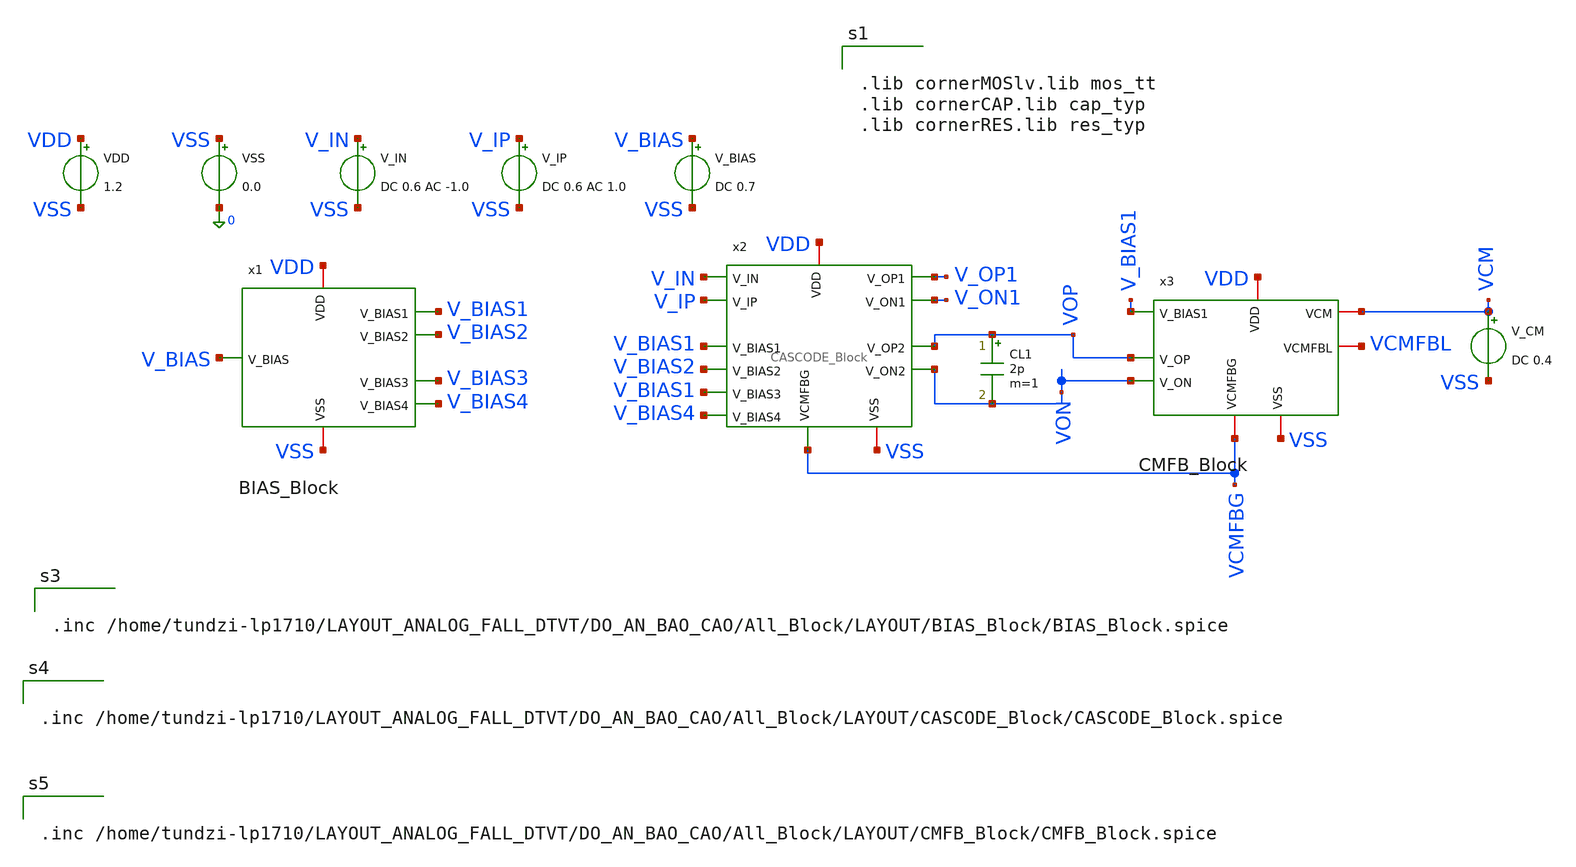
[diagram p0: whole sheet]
** sch_path: two-stage-ota-with-cmfb/Layout_PEX_PostSimulation/LAYOUT/SCHEMATIC_FOR_LAYOUT/All_Block_LAYOUT.sch
**.subckt All_Block_LAYOUT
VDD VDD VSS 1.2
VSS VSS 0 0.0
V_IN V_IN VSS DC 0.6 AC -1.0
V_IP V_IP VSS DC 0.6 AC 1.0
V_BIAS V_BIAS VSS DC 0.7
V_CM VCM VSS DC 0.4
CL1 VOP VON 2p m=1
x1 VDD VSS V_BIAS4 V_BIAS2 V_BIAS3 V_BIAS1 V_BIAS BIAS_Block
x2 VON VOP V_ON1 V_OP1 V_IN V_IP V_BIAS1 VSS V_BIAS4 V_BIAS1 VCMFBG VDD V_BIAS2 CASCODE_Block
x3 VDD V_BIAS1 VOP VON VCM VCMFBG VCMFBL VSS CMFB_Block
**** begin user architecture code


.lib cornerMOSlv.lib mos_tt
.lib cornerCAP.lib cap_typ
.lib cornerRES.lib res_typ




.control
unset echo
set color0=white
set color1=black

* ============================================================
* 1. DC, CONG SUAT & OUTPUT COMMON-MODE
* ============================================================
op
let p_total = -v(VDD)*i(vdd)
let vocm = 0.5 * (v(vop) + v(von))
set r_vocm = $&vocm
set r_ptotal = $&p_total

* ============================================================
* 2. AC VI SAI: GAIN, GBW, PHASE MARGIN
* ============================================================
alter @v_ip[acmag] = 0.5
alter @v_in[acmag] = -0.5
alter @vdd[acmag] = 0

ac dec 50 1 10G
let vod = v(vop) - v(von)
let vid = v(v_ip) - v(v_in)
let gain_db = db(vod/vid)
let phase_deg = 180/PI * cph(vod/vid)

meas ac adm_dc find gain_db at=1
meas ac GBW when gain_db=0
meas ac Phase_at_GBW find phase_deg at=GBW
let Phase_Margin = 180 + Phase_at_GBW

set r_gain = $&adm_dc
set r_gbw_mhz = $&GBW
set r_pm = $&Phase_Margin

* ============================================================
* 3. NOISE NGO VAO TAI 1 MHz (DA SUA TRIET DE LOI SCALAR)
* ============================================================
noise v(vop,von) v_ip dec 10 1Meg 1Meg
let noise_val = noise1.inoise_spectrum
set r_noise = $&noise_val

* ============================================================
* 4. CMRR TAI DC
* ============================================================
alter @v_ip[acmag] = 1.0
alter @v_in[acmag] = 1.0
alter @vdd[acmag] = 0

ac dec 20 1 10Meg
let vocm_ac = 0.5 * (v(vop) + v(von))
let vicm_ac = v(v_ip)
let acm_db = db(vocm_ac / vicm_ac)
let cmrr_val = $r_gain - acm_db[0]
set r_cmrr = $&cmrr_val

* ============================================================
* 5. PSRR TAI DC
* ============================================================
alter @v_ip[acmag] = 0
alter @v_in[acmag] = 0
alter @vdd[acmag] = 1.0

ac dec 20 1 10Meg
let vod_psrr = v(vop) - v(von)
let asupply_db = db(vod_psrr)
let psrr_val = $r_gain - asupply_db[0]
set r_psrr = $&psrr_val

* ============================================================
* 6. TRANSIENT: SLEW RATE & OUTPUT SWING
* ============================================================
alter @vdd[acmag] = 0
alter @v_ip[acmag] = 0
alter @v_in[acmag] = 0

alter @v_ip[pulse] = [ 0.2 1.0 10n 0.1n 0.1n 40n 100n ]
alter @v_in[pulse] = [ 1.0 0.2 10n 0.1n 0.1n 40n 100n ]

tran 0.1n 100n
let v_diff = v(vop) - v(von)

meas tran v_max max v_diff
meas tran v_min min v_diff
let v_diff_pp = v_max - v_min
set r_swing = $&v_diff_pp

meas tran t1 when v_diff=-0.2 cross=1
meas tran t2 when v_diff=0.2 cross=1
let sr_rise = (0.4) / (t2 - t1) / 1e6

meas tran t3 when v_diff=0.2 cross=2
meas tran t4 when v_diff=-0.2 cross=2
let sr_fall = (0.4) / (t4 - t3) / 1e6
let sr_avg = 0.5 * (sr_rise + sr_fall)
set r_sr = $&sr_avg

* ============================================================
* BANG TONG HOP KET QUA HOAN CHINH (FINAL PROJECT)
* ============================================================
echo ''
echo '=========================================================================='
echo '                   TARGET SPECIFICATIONS FINAL PROJECT (POST-LAYOUT)                   '
echo '=========================================================================='
echo '1. DC Gain (dB)          [Target >= 75 dB]      : ' $r_gain 'dB'
echo '2. GBW (Hz)              [Target >= 200 MHz]    : ' $r_gbw_mhz 'Hz'
echo '3. Phase Margin (deg)    [Target >= 60 deg]     : ' $r_pm 'deg'
echo '4. Power (W)             [Target < 3.0 mW]      : ' $r_ptotal 'W'
echo '5. Output CM (V)         [Target = 0.60 V]      : ' $r_vocm 'V'
echo '6. Noise @ 1MHz (V/rtHz) [Target < 15 nV/rtHz]  : ' $r_noise 'V/rtHz'
echo '7. CMRR @ DC (dB)        [Target > 80 dB]       : ' $r_cmrr 'dB'
echo '8. PSRR @ DC (dB)        [Target > 70 dB]       : ' $r_psrr 'dB'
echo '9. Slew Rate (V/us)      [Target > 100 V/us]    : ' $r_sr 'V/us'
echo '10. Output Swing (Vpp)   [Target > 1.0 Vpp]     : ' $r_swing 'Vpp'
echo '=========================================================================='
echo ''

.endc




.inc /home/tundzi-lp1710/LAYOUT_ANALOG_FALL_DTVT/DO_AN_BAO_CAO/All_Block/LAYOUT/BIAS_Block/BIAS_Block.spice




.inc /home/tundzi-lp1710/LAYOUT_ANALOG_FALL_DTVT/DO_AN_BAO_CAO/All_Block/LAYOUT/CASCODE_Block/CASCODE_Block.spice




.inc /home/tundzi-lp1710/LAYOUT_ANALOG_FALL_DTVT/DO_AN_BAO_CAO/All_Block/LAYOUT/CMFB_Block/CMFB_Block.spice


**** end user architecture code
**.ends
.end
